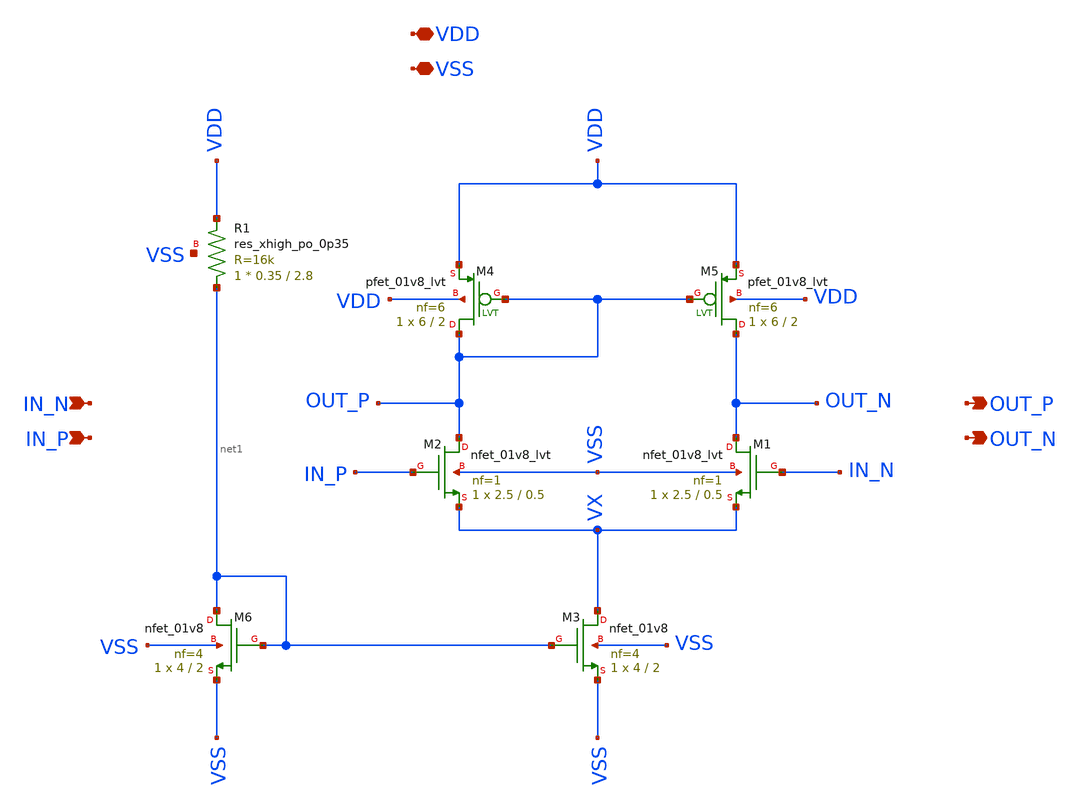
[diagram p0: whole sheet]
** sch_path: xschem/diff_amp.sch
**.subckt diff_amp VDD VSS IN_N IN_P OUT_P OUT_N
*.iopin VDD
*.iopin VSS
*.ipin IN_N
*.ipin IN_P
*.opin OUT_P
*.opin OUT_N
XM3 VX net1 VSS VSS sky130_fd_pr__nfet_01v8 L=2 W=4 nf=4 ad='int((nf+1)/2) * W/nf * 0.29' as='int((nf+2)/2) * W/nf * 0.29'
+ pd='2*int((nf+1)/2) * (W/nf + 0.29)' ps='2*int((nf+2)/2) * (W/nf + 0.29)' nrd='0.29 / W' nrs='0.29 / W'
+ sa=0 sb=0 sd=0 mult=1 m=1
XM6 net1 net1 VSS VSS sky130_fd_pr__nfet_01v8 L=2 W=4 nf=4 ad='int((nf+1)/2) * W/nf * 0.29' as='int((nf+2)/2) * W/nf * 0.29'
+ pd='2*int((nf+1)/2) * (W/nf + 0.29)' ps='2*int((nf+2)/2) * (W/nf + 0.29)' nrd='0.29 / W' nrs='0.29 / W'
+ sa=0 sb=0 sd=0 mult=1 m=1
XR1 net1 VDD VSS sky130_fd_pr__res_xhigh_po_0p35 L=2.8 mult=1 m=1
XM2 OUT_P IN_P VX VSS sky130_fd_pr__nfet_01v8_lvt L=0.5 W=2.5 nf=1 ad='int((nf+1)/2) * W/nf * 0.29' as='int((nf+2)/2) * W/nf * 0.29'
+ pd='2*int((nf+1)/2) * (W/nf + 0.29)' ps='2*int((nf+2)/2) * (W/nf + 0.29)' nrd='0.29 / W' nrs='0.29 / W'
+ sa=0 sb=0 sd=0 mult=1 m=1
XM1 OUT_N IN_N VX VSS sky130_fd_pr__nfet_01v8_lvt L=0.5 W=2.5 nf=1 ad='int((nf+1)/2) * W/nf * 0.29' as='int((nf+2)/2) * W/nf * 0.29'
+ pd='2*int((nf+1)/2) * (W/nf + 0.29)' ps='2*int((nf+2)/2) * (W/nf + 0.29)' nrd='0.29 / W' nrs='0.29 / W'
+ sa=0 sb=0 sd=0 mult=1 m=1
XM4 OUT_P OUT_P VDD VDD sky130_fd_pr__pfet_01v8_lvt L=2 W=6 nf=6 ad='int((nf+1)/2) * W/nf * 0.29' as='int((nf+2)/2) * W/nf * 0.29'
+ pd='2*int((nf+1)/2) * (W/nf + 0.29)' ps='2*int((nf+2)/2) * (W/nf + 0.29)' nrd='0.29 / W' nrs='0.29 / W'
+ sa=0 sb=0 sd=0 mult=1 m=1
XM5 OUT_N OUT_P VDD VDD sky130_fd_pr__pfet_01v8_lvt L=2 W=6 nf=6 ad='int((nf+1)/2) * W/nf * 0.29' as='int((nf+2)/2) * W/nf * 0.29'
+ pd='2*int((nf+1)/2) * (W/nf + 0.29)' ps='2*int((nf+2)/2) * (W/nf + 0.29)' nrd='0.29 / W' nrs='0.29 / W'
+ sa=0 sb=0 sd=0 mult=1 m=1
**.ends
.end
